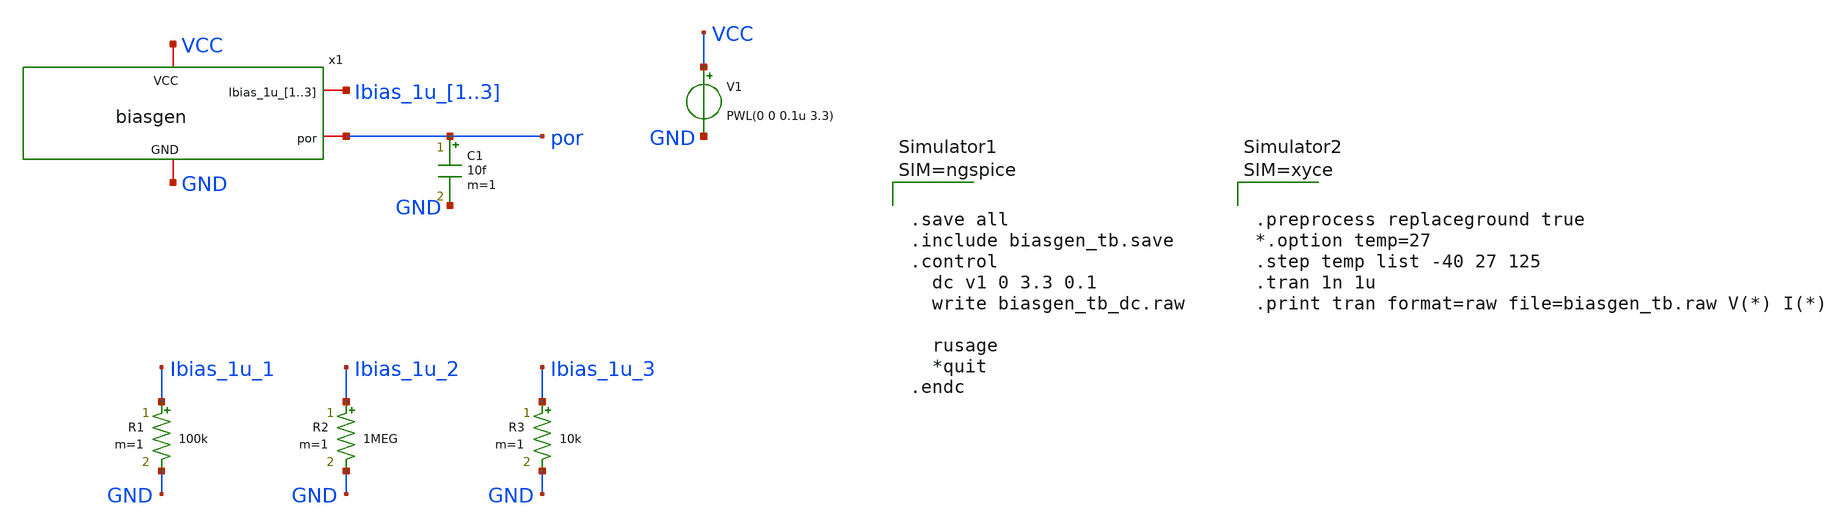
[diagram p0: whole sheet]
** sch_path: FLDO/design_data/xschem/biasgen_tb_dc.sch
**.subckt biasgen_tb_dc
V1 VCC GND PWL(0 0 0.1u 3.3)
x1 VCC GND Ibias_1u_1 Ibias_1u_2 Ibias_1u_3 por biasgen
R1 Ibias_1u_1 GND 100k m=1
R2 Ibias_1u_2 GND 1MEG m=1
R3 Ibias_1u_3 GND 10k m=1
C1 por GND 10f m=1
**** begin user architecture code









** IHP models
.lib cornerMOSlv.lib mos_tt
.lib cornerMOShv.lib mos_tt
.lib cornerHBT.lib hbt_typ
.lib cornerRES.lib res_typ
.lib cornerCAP.lib cap_typ

.include sg13g2_stdcell.spice







.save all
.include biasgen_tb.save
.control
  dc v1 0 3.3 0.1
  write biasgen_tb_dc.raw

  rusage
  *quit
.endc



**** end user architecture code
**.ends

* expanding   symbol:  biasgen.sym # of pins=4
** sym_path: FLDO/design_data/xschem/biasgen.sym
** sch_path: FLDO/design_data/xschem/biasgen.sch
.subckt biasgen VCC GND Ibias_1u_1 Ibias_1u_2 Ibias_1u_3 por
*.iopin VCC
*.iopin GND
*.iopin Ibias_1u_1,Ibias_1u_2,Ibias_1u_3
*.opin por
XM1 vp vn net1 GND sg13_hv_nmos w=2u l=2u ng=1 m=3 mm_ok=1
XM2 vn vn GND GND sg13_hv_nmos w=2u l=2u ng=1 m=1 mm_ok=1
XM3 vn vp VCC VCC sg13_hv_pmos w=0.5u l=2u ng=1 m=2 mm_ok=1
XM4 vp vp VCC VCC sg13_hv_pmos w=0.5u l=2u ng=1 m=2 mm_ok=1
XMout0 Ibias_1u_0 vp VCC VCC sg13_hv_pmos w=0.5u l=2u ng=1 m=1 mm_ok=1
XMout1 Ibias_1u_1 vp VCC VCC sg13_hv_pmos w=0.5u l=2u ng=1 m=1 mm_ok=1
XMout2 Ibias_1u_2 vp VCC VCC sg13_hv_pmos w=0.5u l=2u ng=1 m=1 mm_ok=1
XMout3 Ibias_1u_3 vp VCC VCC sg13_hv_pmos w=0.5u l=2u ng=1 m=1 mm_ok=1
XC1 Ibias_1u_0 GND cap_cmim w=7.0e-6 l=7.0e-6 m=1
XM7 por Ibias_1u_0 VCC VCC sg13_hv_pmos w=0.3u l=0.4u ng=1 m=1 mm_ok=1
XM8 por Ibias_1u_0 GND GND sg13_hv_nmos w=0.3u l=0.45u ng=1 m=1 mm_ok=1
XR1 net1 GND GND rppd w=0.5e-6 l=80e-6 m=1 b=0 mm_ok=1
XM5 vp vstart GND GND sg13_hv_nmos w=0.3u l=0.45u ng=1 m=1 mm_ok=1
XM6 vstart vn GND GND sg13_hv_nmos w=0.3u l=0.45u ng=1 m=1 mm_ok=1
XM9 vstart vn net2 VCC sg13_hv_pmos w=0.3u l=2u ng=1 m=1 mm_ok=1
XM10 net2 net2 net3 VCC sg13_hv_pmos w=0.3u l=2u ng=1 m=1 mm_ok=1
XM11 net3 net3 VCC VCC sg13_hv_pmos w=0.3u l=2u ng=1 m=1 mm_ok=1
.ends

.end
